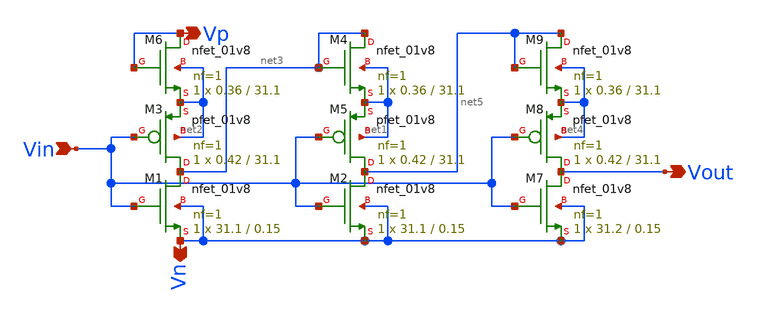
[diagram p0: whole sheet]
** sch_path: xschem/Vth_sch/Symbol/Inverter-th01.sch
**.subckt Inverter-th01 Vin Vout Vp Vn
*.ipin Vin
*.opin Vout
*.opin Vp
*.opin Vn
XM2 net5 Vin Vn Vn sky130_fd_pr__nfet_01v8 L=0.15 W=31.1 nf=1 ad='int((nf+1)/2) * W/nf * 0.29' as='int((nf+2)/2) * W/nf * 0.29'
+ pd='2*int((nf+1)/2) * (W/nf + 0.29)' ps='2*int((nf+2)/2) * (W/nf + 0.29)' nrd='0.29 / W' nrs='0.29 / W'
+ sa=0 sb=0 sd=0 mult=1 m=1
XM5 net5 Vin net1 net1 sky130_fd_pr__pfet_01v8 L=31.1 W=0.42 nf=1 ad='int((nf+1)/2) * W/nf * 0.29' as='int((nf+2)/2) * W/nf * 0.29'
+ pd='2*int((nf+1)/2) * (W/nf + 0.29)' ps='2*int((nf+2)/2) * (W/nf + 0.29)' nrd='0.29 / W' nrs='0.29 / W'
+ sa=0 sb=0 sd=0 mult=1 m=1
XM1 net3 Vin Vn Vn sky130_fd_pr__nfet_01v8 L=0.15 W=31.1 nf=1 ad='int((nf+1)/2) * W/nf * 0.29' as='int((nf+2)/2) * W/nf * 0.29'
+ pd='2*int((nf+1)/2) * (W/nf + 0.29)' ps='2*int((nf+2)/2) * (W/nf + 0.29)' nrd='0.29 / W' nrs='0.29 / W'
+ sa=0 sb=0 sd=0 mult=1 m=1
XM3 net3 Vin net2 net2 sky130_fd_pr__pfet_01v8 L=31.1 W=0.42 nf=1 ad='int((nf+1)/2) * W/nf * 0.29' as='int((nf+2)/2) * W/nf * 0.29'
+ pd='2*int((nf+1)/2) * (W/nf + 0.29)' ps='2*int((nf+2)/2) * (W/nf + 0.29)' nrd='0.29 / W' nrs='0.29 / W'
+ sa=0 sb=0 sd=0 mult=1 m=1
XM4 net3 net3 net1 net1 sky130_fd_pr__nfet_01v8 L=31.1 W=0.36 nf=1 ad='int((nf+1)/2) * W/nf * 0.29' as='int((nf+2)/2) * W/nf * 0.29'
+ pd='2*int((nf+1)/2) * (W/nf + 0.29)' ps='2*int((nf+2)/2) * (W/nf + 0.29)' nrd='0.29 / W' nrs='0.29 / W'
+ sa=0 sb=0 sd=0 mult=1 m=1
XM6 Vp Vp net2 net2 sky130_fd_pr__nfet_01v8 L=31.1 W=0.36 nf=1 ad='int((nf+1)/2) * W/nf * 0.29' as='int((nf+2)/2) * W/nf * 0.29'
+ pd='2*int((nf+1)/2) * (W/nf + 0.29)' ps='2*int((nf+2)/2) * (W/nf + 0.29)' nrd='0.29 / W' nrs='0.29 / W'
+ sa=0 sb=0 sd=0 mult=1 m=1
XM7 Vout Vin Vn Vn sky130_fd_pr__nfet_01v8 L=0.15 W=31.2 nf=1 ad='int((nf+1)/2) * W/nf * 0.29' as='int((nf+2)/2) * W/nf * 0.29'
+ pd='2*int((nf+1)/2) * (W/nf + 0.29)' ps='2*int((nf+2)/2) * (W/nf + 0.29)' nrd='0.29 / W' nrs='0.29 / W'
+ sa=0 sb=0 sd=0 mult=1 m=1
XM8 Vout Vin net4 net4 sky130_fd_pr__pfet_01v8 L=31.1 W=0.42 nf=1 ad='int((nf+1)/2) * W/nf * 0.29' as='int((nf+2)/2) * W/nf * 0.29'
+ pd='2*int((nf+1)/2) * (W/nf + 0.29)' ps='2*int((nf+2)/2) * (W/nf + 0.29)' nrd='0.29 / W' nrs='0.29 / W'
+ sa=0 sb=0 sd=0 mult=1 m=1
XM9 net5 net5 net4 net4 sky130_fd_pr__nfet_01v8 L=31.1 W=0.36 nf=1 ad='int((nf+1)/2) * W/nf * 0.29' as='int((nf+2)/2) * W/nf * 0.29'
+ pd='2*int((nf+1)/2) * (W/nf + 0.29)' ps='2*int((nf+2)/2) * (W/nf + 0.29)' nrd='0.29 / W' nrs='0.29 / W'
+ sa=0 sb=0 sd=0 mult=1 m=1
**.ends
.end
